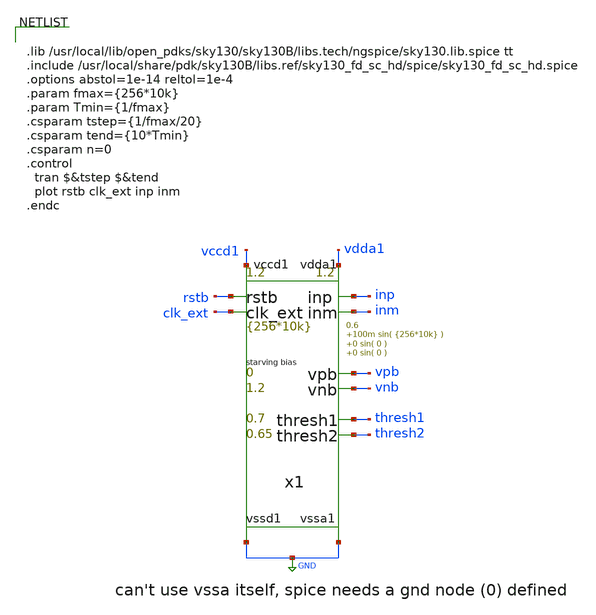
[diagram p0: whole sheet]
** sch_path: xschem/test_bench/pad_frame_tb.sch
**.subckt pad_frame_tb
x1 thresh1 thresh2 vdda1 GND inp inm clk_ext rstb vccd1 GND vpb vnb pad_frame p_vdda1=1.2 p_vccd1=1.2
+ p_fclk={256*10k} p_duty_cycle=0.5 p_rstb_delay={1.5/p_fclk} p_rstb_tr=5n p_thresh1=0.7 p_thresh2=0.65
+ p_vpb=0 p_vnb=1.2 p_vcm=0.6 p_amp1=100m p_f1={256*10k} p_amp2=0 p_f2=0 p_amp3=0 p_f3=0
**** begin user architecture code


.lib /usr/local/lib/open_pdks/sky130/sky130B/libs.tech/ngspice/sky130.lib.spice tt
.include /usr/local/share/pdk/sky130B/libs.ref/sky130_fd_sc_hd/spice/sky130_fd_sc_hd.spice
.options abstol=1e-14 reltol=1e-4
.param fmax={256*10k}
.param Tmin={1/fmax}
.csparam tstep={1/fmax/20}
.csparam tend={10*Tmin}
.csparam n=0
.control
  tran $&tstep $&tend
  plot rstb clk_ext inp inm
.endc


**** end user architecture code
**.ends

* expanding   symbol:  test_bench/pad_frame.sym # of pins=12
** sym_path: xschem/test_bench/pad_frame.sym
** sch_path: xschem/test_bench/pad_frame.sch
.subckt pad_frame thresh1 thresh2 vdda1 vssa1 inp inm clk_ext rstb vccd1 vssd1 vpb vnb   p_vdda1=1.2
+  p_vccd1=1.2  p_fclk={256*10k}  p_duty_cycle=0.5  p_rstb_delay={1.5/p_fclk}  p_rstb_tr=5n  p_thresh1=0.7
+  p_thresh2=0.65  p_vpb=0  p_vnb=1.2  p_vcm=0.6  p_amp1=100m  p_f1={256*10k}  p_amp2=0  p_f2=0  p_amp3=0
+  p_f3=0
*.opin thresh1
*.opin thresh2
*.opin vdda1
*.opin vssa1
*.opin inp
*.opin inm
*.opin vccd1
*.opin vssd1
*.opin rstb
*.opin clk_ext
*.opin vpb
*.opin vnb
vdda1 vdda1 vssa1 DC {p_vdda1}
vthresh1 thresh1 vssa1 DC {p_thresh1}
vthresh2 thresh2 vssa1 DC {p_thresh2}
vinp1 inp inp2 DC 0 SIN(0 {p_amp1} {p_f1})
vinm1 inm inm2 DC 0 SIN(0 {-p_amp1} {p_f1})
vpb vpb vssa1 DC {p_vpb}
vnb vnb vssa1 DC {p_vnb}
vinp2 inp2 inp3 DC 0 SIN(0 {p_amp2} {p_f2})
vinp3 inp3 vcm DC 0 SIN(0 {p_amp3} {p_f3})
vinm2 inm2 inm3 DC 0 SIN(0 {-p_amp2} {p_f2})
vinm3 inm3 vcm DC 0 SIN(0 {-p_amp3} {p_f3})
vcm vcm vssa1 DC {p_vcm}
vdda2 vccd1 vssd1 DC {p_vccd1}
Vclk clk vssd1 DC 0 PULSE (0 p_vccd1 1n 1n 1n {p_duty_cycle*1/p_fclk} {1/p_fclk} 0
Vrstb rstb vssd1 DC 0 PWL ( 0 0 p_rstb_delay 0 {p_rstb_delay + p_rstb_tr} p_vccd1)
x1 clk rstb vssd1 vssd1 vccd1 vccd1 clk_ext sky130_fd_sc_hd__dlclkp_1
.ends

.GLOBAL GND
.end
